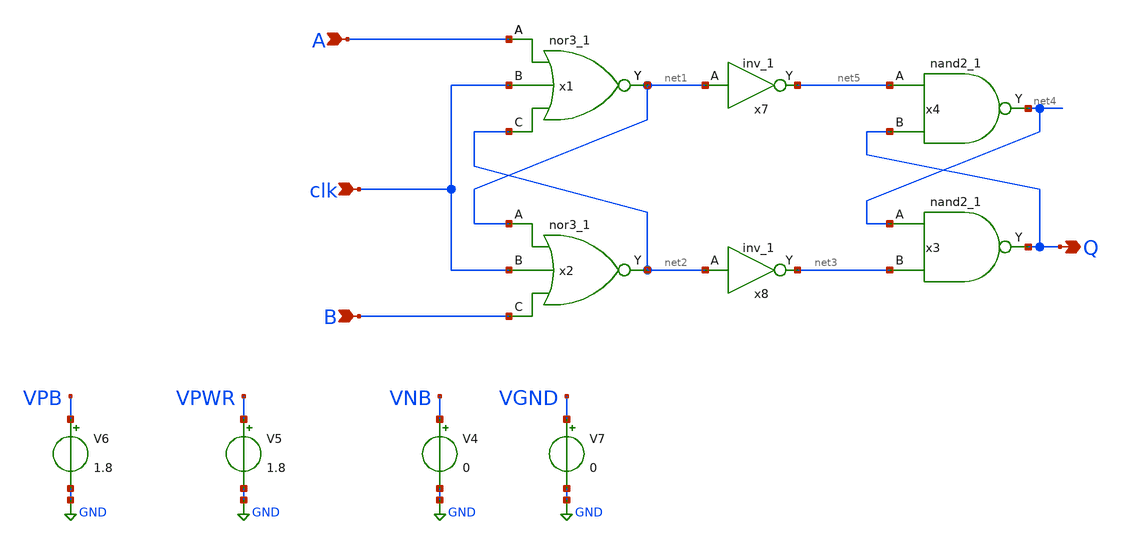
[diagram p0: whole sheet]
** sch_path: NORcmp.sch
**.subckt NORcmp A clk B Q
*.ipin A
*.ipin clk
*.ipin B
*.opin Q
x7 net1 VGND VNB VPB VPWR net5 sky130_fd_sc_hd__inv_1
x8 net2 VGND VNB VPB VPWR net3 sky130_fd_sc_hd__inv_1
x1 A clk net2 VGND VNB VPB VPWR net1 sky130_fd_sc_hd__nor3_1
x2 net1 clk B VGND VNB VPB VPWR net2 sky130_fd_sc_hd__nor3_1
x4 net5 Q VGND VNB VPB VPWR net4 sky130_fd_sc_hd__nand2_1
x3 net4 net3 VGND VNB VPB VPWR Q sky130_fd_sc_hd__nand2_1
V4 VNB GND 0
V5 VPWR GND 1.8
V6 VPB GND 1.8
V7 VGND GND 0
**.ends
.GLOBAL GND
.end
